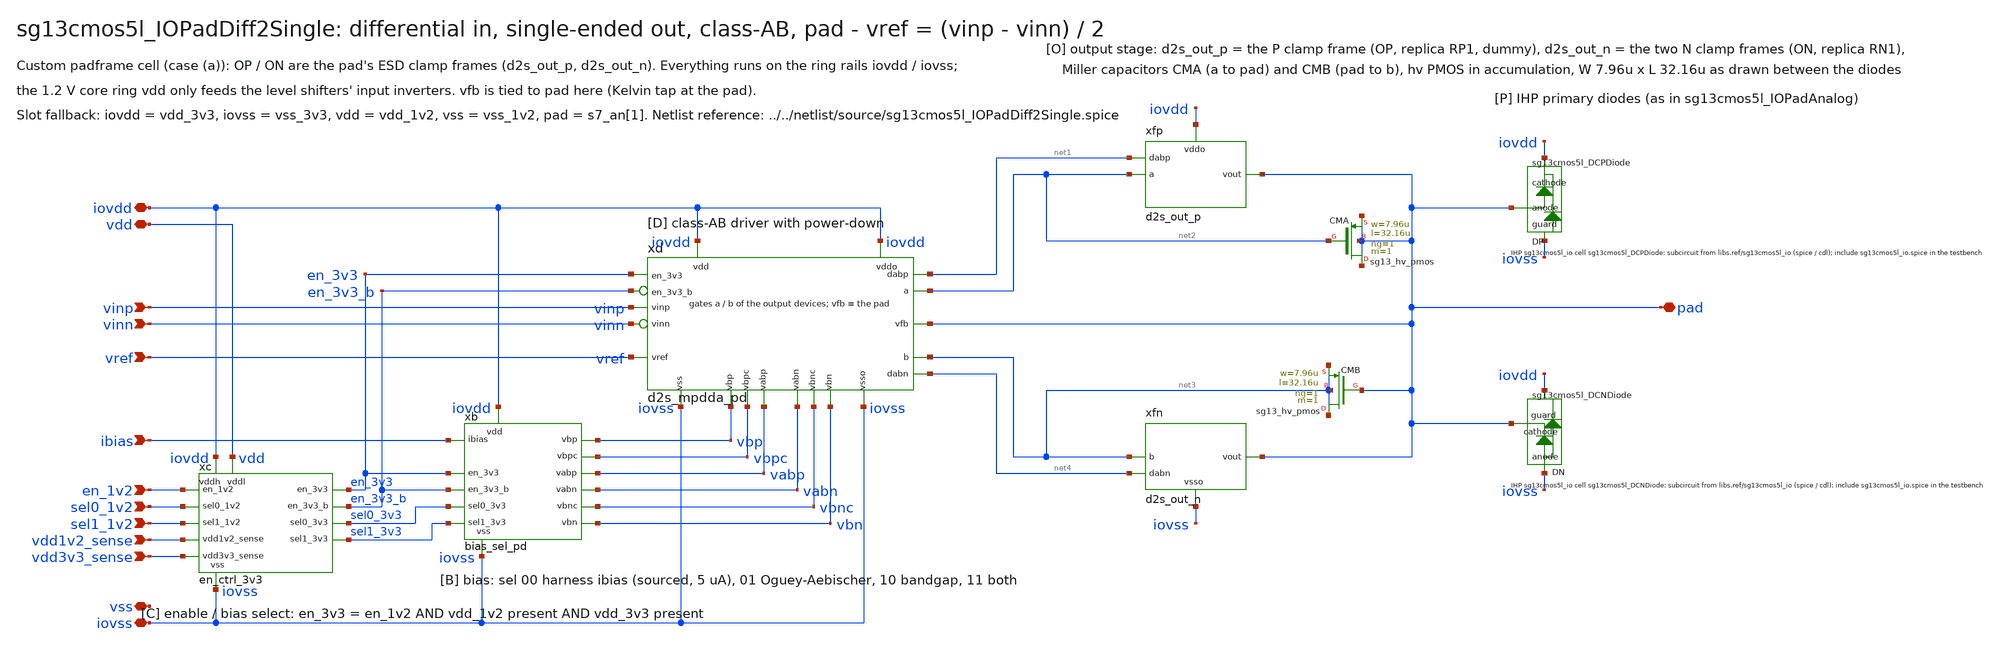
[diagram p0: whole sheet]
** sch_path: macros/sg13cmos5l_IOPadDiff2Single/schematic/xschem/sg13cmos5l_IOPadDiff2Single.sch
**.subckt sg13cmos5l_IOPadDiff2Single iovdd iovss vdd vss vinp vinn vref ibias en_1v2 sel0_1v2
*+ sel1_1v2 vdd1v2_sense vdd3v3_sense pad
*.iopin iovdd
*.iopin iovss
*.iopin vdd
*.iopin vss
*.ipin vinp
*.ipin vinn
*.ipin vref
*.ipin ibias
*.ipin en_1v2
*.ipin sel0_1v2
*.ipin sel1_1v2
*.ipin vdd1v2_sense
*.ipin vdd3v3_sense
*.iopin pad
xc iovdd vdd iovss en_1v2 sel0_1v2 sel1_1v2 vdd1v2_sense vdd3v3_sense en_3v3 sel0_3v3 sel1_3v3
+ en_3v3_b en_ctrl_3v3
xb iovdd iovss ibias vbp vbn vbpc vbnc vabp vabn en_3v3 sel0_3v3 sel1_3v3 en_3v3_b bias_sel_pd
xd iovdd iovss iovdd iovss vinp vinn vref pad net2 net3 net1 net4 vbp vbn vbpc vbnc vabp vabn en_3v3
+ en_3v3_b d2s_mpdda_pd
xfp iovdd net2 pad net1 d2s_out_p
xfn iovss net3 pad net4 d2s_out_n
XCMA pad net2 pad pad sg13_hv_pmos w=7.96u l=32.16u ng=1 m=1 mm_ok=1
XCMB net3 pad net3 net3 sg13_hv_pmos w=7.96u l=32.16u ng=1 m=1 mm_ok=1
XDP pad iovdd iovss sg13cmos5l_DCPDiode
XDN iovss pad iovdd sg13cmos5l_DCNDiode
**.ends
.end
